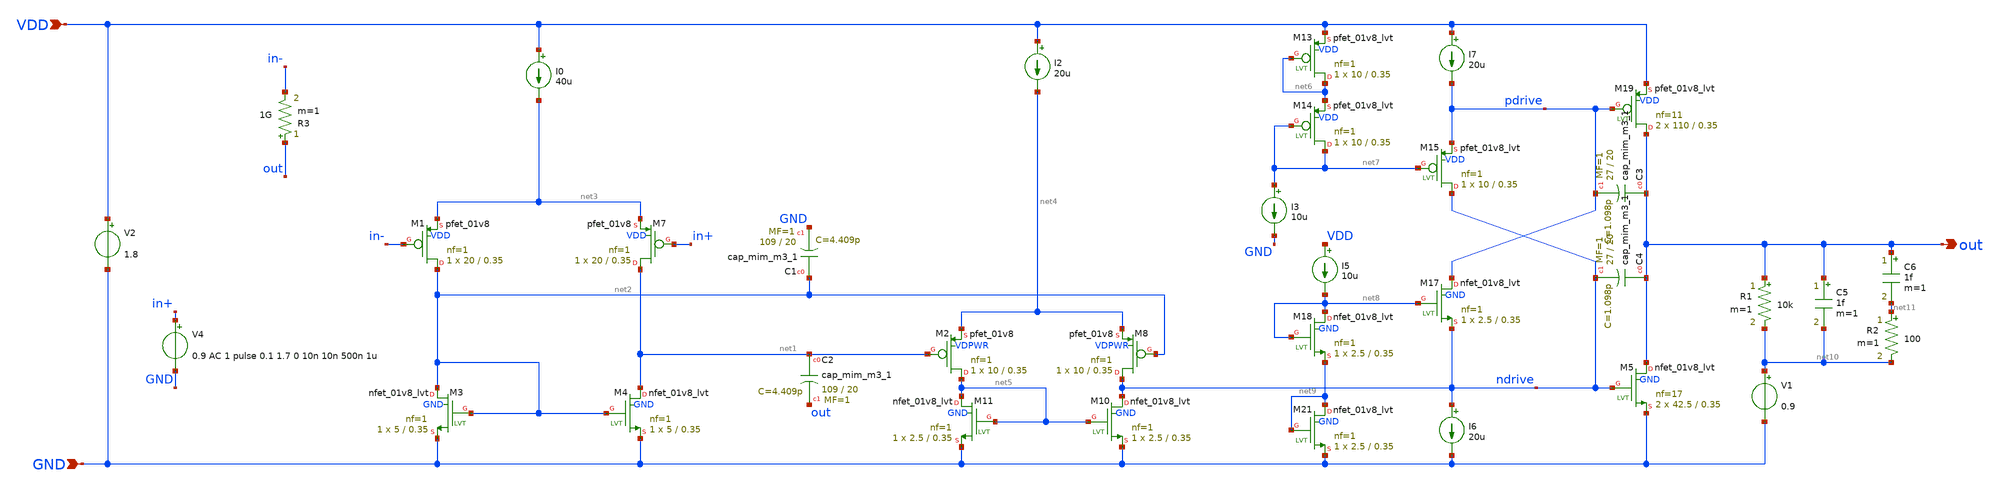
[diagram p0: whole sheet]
** sch_path: xschem/Rod_Design.sch
**.subckt Rod_Design GND VDD out
*.ipin GND
*.ipin VDD
*.opin out
I0 VDD net3 40u
XC1 net2 GND sky130_fd_pr__cap_mim_m3_1 W=109 L=20 MF=1 m=1
XC2 net1 out sky130_fd_pr__cap_mim_m3_1 W=109 L=20 MF=1 m=1
I2 VDD net4 20u
XM13 net6 net6 VDD VDD sky130_fd_pr__pfet_01v8_lvt L=0.35 W=10 nf=1 ad='int((nf+1)/2) * W/nf * 0.29'
+ as='int((nf+2)/2) * W/nf * 0.29' pd='2*int((nf+1)/2) * (W/nf + 0.29)' ps='2*int((nf+2)/2) * (W/nf + 0.29)'
+ nrd='0.29 / W' nrs='0.29 / W' sa=0 sb=0 sd=0 mult=1 m=1
XM14 net7 net7 net6 VDD sky130_fd_pr__pfet_01v8_lvt L=0.35 W=10 nf=1 ad='int((nf+1)/2) * W/nf * 0.29'
+ as='int((nf+2)/2) * W/nf * 0.29' pd='2*int((nf+1)/2) * (W/nf + 0.29)' ps='2*int((nf+2)/2) * (W/nf + 0.29)'
+ nrd='0.29 / W' nrs='0.29 / W' sa=0 sb=0 sd=0 mult=1 m=1
XM15 ndrive net7 pdrive VDD sky130_fd_pr__pfet_01v8_lvt L=0.35 W=10 nf=1 ad='int((nf+1)/2) * W/nf * 0.29'
+ as='int((nf+2)/2) * W/nf * 0.29' pd='2*int((nf+1)/2) * (W/nf + 0.29)' ps='2*int((nf+2)/2) * (W/nf + 0.29)'
+ nrd='0.29 / W' nrs='0.29 / W' sa=0 sb=0 sd=0 mult=1 m=1
I3 net7 GND 10u
I5 VDD net8 10u
I6 ndrive GND 20u
XM19 out pdrive VDD VDD sky130_fd_pr__pfet_01v8_lvt L=0.35 W=110 nf=11 ad='int((nf+1)/2) * W/nf * 0.29'
+ as='int((nf+2)/2) * W/nf * 0.29' pd='2*int((nf+1)/2) * (W/nf + 0.29)' ps='2*int((nf+2)/2) * (W/nf + 0.29)'
+ nrd='0.29 / W' nrs='0.29 / W' sa=0 sb=0 sd=0 mult=2 m=2
I7 VDD pdrive 20u
XC3 out pdrive sky130_fd_pr__cap_mim_m3_1 W=27 L=20 MF=1 m=1
XC4 out ndrive sky130_fd_pr__cap_mim_m3_1 W=27 L=20 MF=1 m=1
R1 out net10 10k m=1
C5 out net10 1f m=1
V1 net10 GND 0.9
R2 net11 net10 100 m=1
C6 out net11 1f m=1
XM21 net9 net9 GND GND sky130_fd_pr__nfet_01v8_lvt L=0.35 W=2.5 nf=1 ad='int((nf+1)/2) * W/nf * 0.29'
+ as='int((nf+2)/2) * W/nf * 0.29' pd='2*int((nf+1)/2) * (W/nf + 0.29)' ps='2*int((nf+2)/2) * (W/nf + 0.29)'
+ nrd='0.29 / W' nrs='0.29 / W' sa=0 sb=0 sd=0 mult=1 m=1
XM3 net2 net2 GND GND sky130_fd_pr__nfet_01v8_lvt L=0.35 W=5 nf=1 ad='int((nf+1)/2) * W/nf * 0.29' as='int((nf+2)/2) * W/nf * 0.29'
+ pd='2*int((nf+1)/2) * (W/nf + 0.29)' ps='2*int((nf+2)/2) * (W/nf + 0.29)' nrd='0.29 / W' nrs='0.29 / W'
+ sa=0 sb=0 sd=0 mult=1 m=1
XM4 net1 net2 GND GND sky130_fd_pr__nfet_01v8_lvt L=0.35 W=5 nf=1 ad='int((nf+1)/2) * W/nf * 0.29' as='int((nf+2)/2) * W/nf * 0.29'
+ pd='2*int((nf+1)/2) * (W/nf + 0.29)' ps='2*int((nf+2)/2) * (W/nf + 0.29)' nrd='0.29 / W' nrs='0.29 / W'
+ sa=0 sb=0 sd=0 mult=1 m=1
XM10 ndrive net5 GND GND sky130_fd_pr__nfet_01v8_lvt L=0.35 W=2.5 nf=1 ad='int((nf+1)/2) * W/nf * 0.29'
+ as='int((nf+2)/2) * W/nf * 0.29' pd='2*int((nf+1)/2) * (W/nf + 0.29)' ps='2*int((nf+2)/2) * (W/nf + 0.29)'
+ nrd='0.29 / W' nrs='0.29 / W' sa=0 sb=0 sd=0 mult=1 m=1
XM11 net5 net5 GND GND sky130_fd_pr__nfet_01v8_lvt L=0.35 W=2.5 nf=1 ad='int((nf+1)/2) * W/nf * 0.29'
+ as='int((nf+2)/2) * W/nf * 0.29' pd='2*int((nf+1)/2) * (W/nf + 0.29)' ps='2*int((nf+2)/2) * (W/nf + 0.29)'
+ nrd='0.29 / W' nrs='0.29 / W' sa=0 sb=0 sd=0 mult=1 m=1
XM17 pdrive net8 ndrive GND sky130_fd_pr__nfet_01v8_lvt L=0.35 W=2.5 nf=1 ad='int((nf+1)/2) * W/nf * 0.29'
+ as='int((nf+2)/2) * W/nf * 0.29' pd='2*int((nf+1)/2) * (W/nf + 0.29)' ps='2*int((nf+2)/2) * (W/nf + 0.29)'
+ nrd='0.29 / W' nrs='0.29 / W' sa=0 sb=0 sd=0 mult=1 m=1
XM18 net8 net8 net9 GND sky130_fd_pr__nfet_01v8_lvt L=0.35 W=2.5 nf=1 ad='int((nf+1)/2) * W/nf * 0.29'
+ as='int((nf+2)/2) * W/nf * 0.29' pd='2*int((nf+1)/2) * (W/nf + 0.29)' ps='2*int((nf+2)/2) * (W/nf + 0.29)'
+ nrd='0.29 / W' nrs='0.29 / W' sa=0 sb=0 sd=0 mult=1 m=1
V4 in+ GND 0.9 AC 1 pulse 0.1 1.7 0 10n 10n 500n 1u
R3 out in- 1G m=1
V2 VDD GND 1.8
XM1 net2 in- net3 VDD sky130_fd_pr__pfet_01v8 L=0.35 W=20 nf=1 ad='int((nf+1)/2) * W/nf * 0.29' as='int((nf+2)/2) * W/nf * 0.29'
+ pd='2*int((nf+1)/2) * (W/nf + 0.29)' ps='2*int((nf+2)/2) * (W/nf + 0.29)' nrd='0.29 / W' nrs='0.29 / W'
+ sa=0 sb=0 sd=0 mult=1 m=1
XM7 net1 in+ net3 VDD sky130_fd_pr__pfet_01v8 L=0.35 W=20 nf=1 ad='int((nf+1)/2) * W/nf * 0.29' as='int((nf+2)/2) * W/nf * 0.29'
+ pd='2*int((nf+1)/2) * (W/nf + 0.29)' ps='2*int((nf+2)/2) * (W/nf + 0.29)' nrd='0.29 / W' nrs='0.29 / W'
+ sa=0 sb=0 sd=0 mult=1 m=1
XM2 net5 net1 net4 VDPWR sky130_fd_pr__pfet_01v8 L=0.35 W=10 nf=1 ad='int((nf+1)/2) * W/nf * 0.29' as='int((nf+2)/2) * W/nf * 0.29'
+ pd='2*int((nf+1)/2) * (W/nf + 0.29)' ps='2*int((nf+2)/2) * (W/nf + 0.29)' nrd='0.29 / W' nrs='0.29 / W'
+ sa=0 sb=0 sd=0 mult=1 m=1
XM8 ndrive net2 net4 VDPWR sky130_fd_pr__pfet_01v8 L=0.35 W=10 nf=1 ad='int((nf+1)/2) * W/nf * 0.29'
+ as='int((nf+2)/2) * W/nf * 0.29' pd='2*int((nf+1)/2) * (W/nf + 0.29)' ps='2*int((nf+2)/2) * (W/nf + 0.29)'
+ nrd='0.29 / W' nrs='0.29 / W' sa=0 sb=0 sd=0 mult=1 m=1
XM5 out ndrive GND GND sky130_fd_pr__nfet_01v8_lvt L=0.35 W=42.5 nf=17 ad='int((nf+1)/2) * W/nf * 0.29'
+ as='int((nf+2)/2) * W/nf * 0.29' pd='2*int((nf+1)/2) * (W/nf + 0.29)' ps='2*int((nf+2)/2) * (W/nf + 0.29)'
+ nrd='0.29 / W' nrs='0.29 / W' sa=0 sb=0 sd=0 mult=2 m=2
**** begin user architecture code



.option reltol=1e-5   abstol=1e-14 savecurrents
.control
  save all
  op
  remzerovec
  write Rod_Design.raw
  set appendwrite
  ac dec 20 1 1e12
  remzerovec
  write Rod_Design.raw
  tran 1e-15 6e-12
  write Rod_Design.raw
.endc




** opencircuitdesign pdks install
.lib $::SKYWATER_MODELS/sky130.lib.spice tt


**** end user architecture code
**.ends
.end
